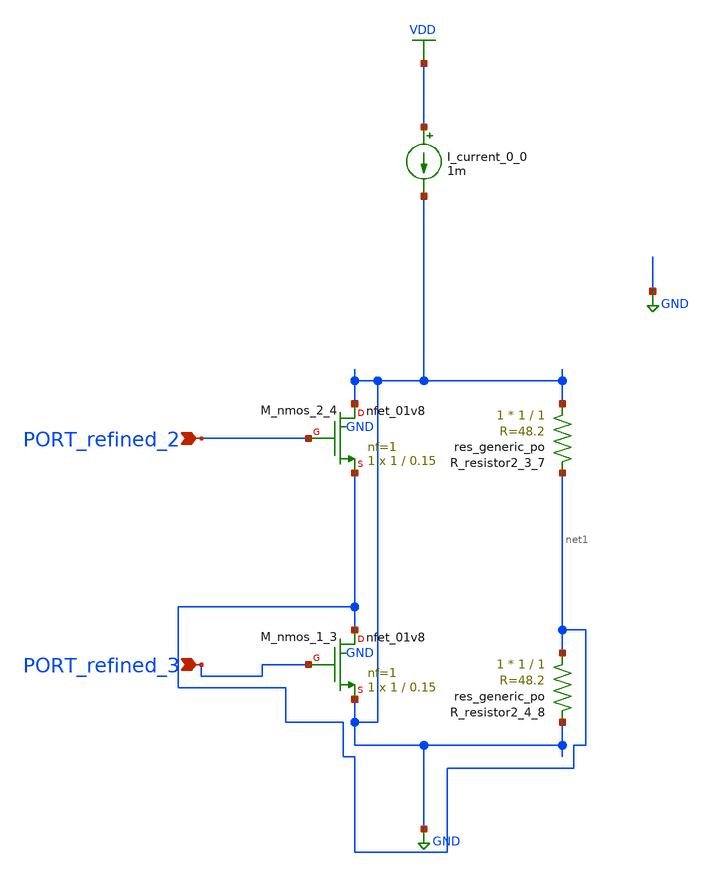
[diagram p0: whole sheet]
** sch_path: schematics/AMSNet/135.sch
**.subckt 135 PORT_refined_3 PORT_refined_2
*.ipin PORT_refined_3
*.ipin PORT_refined_2
I_current_0_0 VDD GND 1m
XM_nmos_1_3 net1 PORT_refined_3 GND GND sky130_fd_pr__nfet_01v8 L=0.15 W=1 nf=1 ad='int((1 + 1)/2) * 1 / 1 * 0.29'
+ as='int((1 + 2)/2) * 1 / 1 * 0.29' pd='2*int((1 + 1)/2) * (1 / 1 + 0.29)' ps='2*int((1 + 2)/2) * (1 / 1 + 0.29)'
+ nrd='0.29 / 1 ' nrs='0.29 / 1 ' sa=0 sb=0 sd=0 mult=1 m=1
XM_nmos_2_4 GND PORT_refined_2 net1 GND sky130_fd_pr__nfet_01v8 L=0.15 W=1 nf=1 ad='int((1 + 1)/2) * 1 / 1 * 0.29'
+ as='int((1 + 2)/2) * 1 / 1 * 0.29' pd='2*int((1 + 1)/2) * (1 / 1 + 0.29)' ps='2*int((1 + 2)/2) * (1 / 1 + 0.29)'
+ nrd='0.29 / 1 ' nrs='0.29 / 1 ' sa=0 sb=0 sd=0 mult=1 m=1
XR_resistor2_3_7 GND net1 sky130_fd_pr__res_generic_po W=1 L=1 m=1
XR_resistor2_4_8 net1 GND sky130_fd_pr__res_generic_po W=1 L=1 m=1
**.ends
.GLOBAL GND
.GLOBAL VDD
.end
